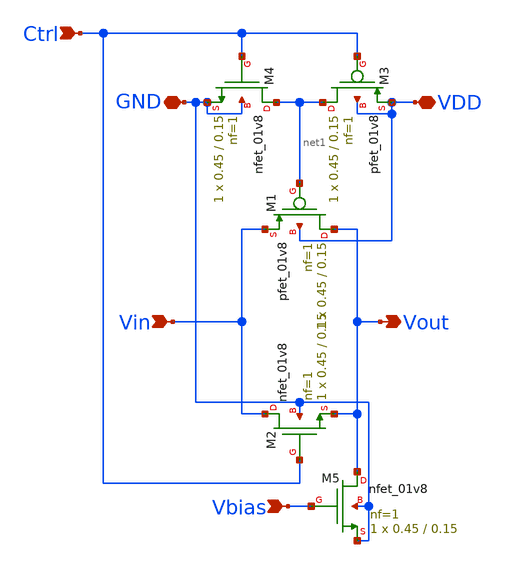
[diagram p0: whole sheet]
** sch_path: SNN/WU_Circuit.sch
**.subckt WU_Circuit GND VDD Vout Ctrl Vin Vbias
*.iopin GND
*.iopin VDD
*.opin Vout
*.ipin Ctrl
*.ipin Vin
*.ipin Vbias
XM1 Vout net1 Vin VDD sky130_fd_pr__pfet_01v8 L=0.15 W=0.45 nf=1 ad='int((nf+1)/2) * W/nf * 0.29' as='int((nf+2)/2) * W/nf * 0.29'
+ pd='2*int((nf+1)/2) * (W/nf + 0.29)' ps='2*int((nf+2)/2) * (W/nf + 0.29)' nrd='0.29 / W' nrs='0.29 / W'
+ sa=0 sb=0 sd=0 mult=1 m=1
XM2 Vin Ctrl Vout GND sky130_fd_pr__nfet_01v8 L=0.15 W=0.45 nf=1 ad='int((nf+1)/2) * W/nf * 0.29' as='int((nf+2)/2) * W/nf * 0.29'
+ pd='2*int((nf+1)/2) * (W/nf + 0.29)' ps='2*int((nf+2)/2) * (W/nf + 0.29)' nrd='0.29 / W' nrs='0.29 / W'
+ sa=0 sb=0 sd=0 mult=1 m=1
XM3 net1 Ctrl VDD VDD sky130_fd_pr__pfet_01v8 L=0.15 W=0.45 nf=1 ad='int((nf+1)/2) * W/nf * 0.29' as='int((nf+2)/2) * W/nf * 0.29'
+ pd='2*int((nf+1)/2) * (W/nf + 0.29)' ps='2*int((nf+2)/2) * (W/nf + 0.29)' nrd='0.29 / W' nrs='0.29 / W'
+ sa=0 sb=0 sd=0 mult=1 m=1
XM4 net1 Ctrl GND GND sky130_fd_pr__nfet_01v8 L=0.15 W=0.45 nf=1 ad='int((nf+1)/2) * W/nf * 0.29' as='int((nf+2)/2) * W/nf * 0.29'
+ pd='2*int((nf+1)/2) * (W/nf + 0.29)' ps='2*int((nf+2)/2) * (W/nf + 0.29)' nrd='0.29 / W' nrs='0.29 / W'
+ sa=0 sb=0 sd=0 mult=1 m=1
XM5 Vout Vbias GND GND sky130_fd_pr__nfet_01v8 L=0.15 W=0.45 nf=1 ad='int((nf+1)/2) * W/nf * 0.29' as='int((nf+2)/2) * W/nf * 0.29'
+ pd='2*int((nf+1)/2) * (W/nf + 0.29)' ps='2*int((nf+2)/2) * (W/nf + 0.29)' nrd='0.29 / W' nrs='0.29 / W'
+ sa=0 sb=0 sd=0 mult=1 m=1
**.ends
.end
